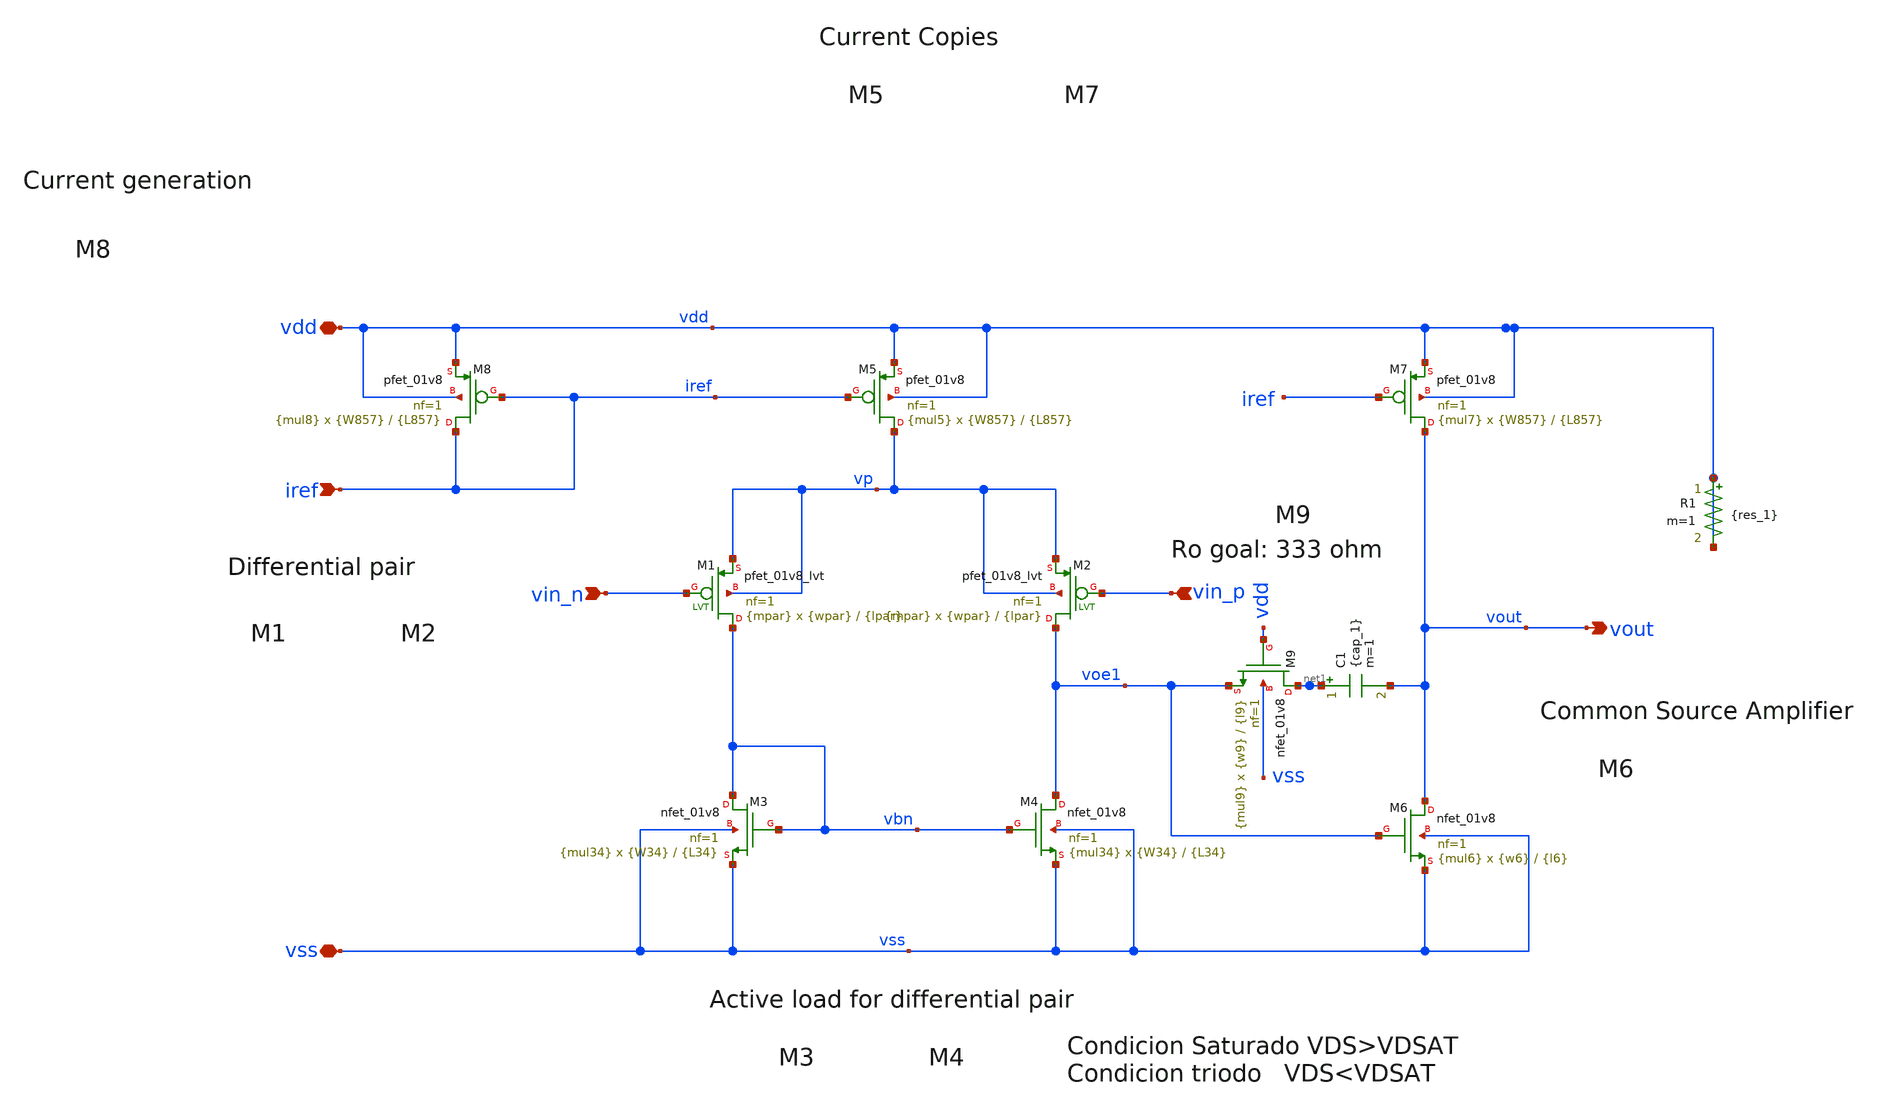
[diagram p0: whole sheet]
** sch_path: opamp.sch
**.subckt opamp vdd vss vin_n vin_p iref vout
*.iopin vdd
*.iopin vss
*.ipin vin_n
*.ipin vin_p
*.ipin iref
*.opin vout
XM3 vbn vbn vss vss sky130_fd_pr__nfet_01v8 L={L34} W={W34} nf=1 ad='W * 0.29' as='W * 0.29' pd='2 * (W + 0.29)'
+ ps='2 * (W + 0.29)' nrd='0.29 / W' nrs='0.29 / W' sa=0 sb=0 sd=0 mult={mul34} m={mul34}
XM4 voe1 vbn vss vss sky130_fd_pr__nfet_01v8 L={L34} W={W34} nf=1 ad='W * 0.29' as='W * 0.29' pd='2 * (W + 0.29)'
+ ps='2 * (W + 0.29)' nrd='0.29 / W' nrs='0.29 / W' sa=0 sb=0 sd=0 mult={mul34} m={mul34}
XM5 vp iref vdd vdd sky130_fd_pr__pfet_01v8 L={L857} W={W857} nf=1 ad='W * 0.29' as='W * 0.29' pd='2 * (W + 0.29)'
+ ps='2 * (W + 0.29)' nrd='0.29 / W' nrs='0.29 / W' sa=0 sb=0 sd=0 mult={mul5} m={mul5}
XM7 vout iref vdd vdd sky130_fd_pr__pfet_01v8 L={L857} W={W857} nf=1 ad='W * 0.29' as='W * 0.29' pd='2 * (W + 0.29)'
+ ps='2 * (W + 0.29)' nrd='0.29 / W' nrs='0.29 / W' sa=0 sb=0 sd=0 mult={mul7} m={mul7}
XM8 iref iref vdd vdd sky130_fd_pr__pfet_01v8 L={L857} W={W857} nf=1 ad='W * 0.29' as='W * 0.29' pd='2 * (W + 0.29)'
+ ps='2 * (W + 0.29)' nrd='0.29 / W' nrs='0.29 / W' sa=0 sb=0 sd=0 mult={mul8} m={mul8}
XM9 net1 vdd voe1 vss sky130_fd_pr__nfet_01v8 L={l9} W={w9} nf=1 ad='W * 0.29' as='W * 0.29' pd='2 * (W + 0.29)'
+ ps='2 * (W + 0.29)' nrd='0.29 / W' nrs='0.29 / W' sa=0 sb=0 sd=0 mult={mul9} m={mul9}
XM6 vout voe1 vss vss sky130_fd_pr__nfet_01v8 L={l6} W={w6} nf=1 ad='W * 0.29' as='W * 0.29' pd='2 * (W + 0.29)'
+ ps='2 * (W + 0.29)' nrd='0.29 / W' nrs='0.29 / W' sa=0 sb=0 sd=0 mult={mul6} m={mul6}
XM1 vbn vin_n vp vp sky130_fd_pr__pfet_01v8_lvt L={lpar} W={wpar} nf=1 ad='int((nf+1)/2) * W/nf * 0.29'
+ as='int((nf+2)/2) * W/nf * 0.29' pd='2*int((nf+1)/2) * (W/nf + 0.29)' ps='2*int((nf+2)/2) * (W/nf + 0.29)'
+ nrd='0.29 / W' nrs='0.29 / W' sa=0 sb=0 sd=0 mult={mpar} m={mpar}
XM2 voe1 vin_p vp vp sky130_fd_pr__pfet_01v8_lvt L={lpar} W={wpar} nf=1 ad='int((nf+1)/2) * W/nf * 0.29'
+ as='int((nf+2)/2) * W/nf * 0.29' pd='2*int((nf+1)/2) * (W/nf + 0.29)' ps='2*int((nf+2)/2) * (W/nf + 0.29)'
+ nrd='0.29 / W' nrs='0.29 / W' sa=0 sb=0 sd=0 mult={mpar} m={mpar}
C1 net1 vout {cap_1} m=1
R1 vdd vdd {res_1} m=1
**.ends
.end
